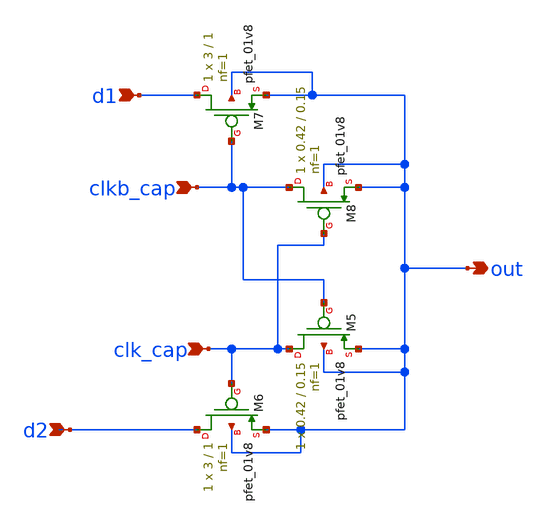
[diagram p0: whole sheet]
** sch_path: xschem/pmos_cp1.sch
**.subckt pmos_cp1 out clkb_cap d1 d2 clk_cap
*.opin out
*.ipin clkb_cap
*.ipin d1
*.ipin d2
*.ipin clk_cap
XM5 clk_cap clkb_cap out out sky130_fd_pr__pfet_01v8 L=0.15 W=0.42 nf=1 ad='int((nf+1)/2) * W/nf * 0.29'
+ as='int((nf+2)/2) * W/nf * 0.29' pd='2*int((nf+1)/2) * (W/nf + 0.29)' ps='2*int((nf+2)/2) * (W/nf + 0.29)'
+ nrd='0.29 / W' nrs='0.29 / W' sa=0 sb=0 sd=0 mult=1 m=1
XM6 d2 clk_cap out out sky130_fd_pr__pfet_01v8 L=1 W=3 nf=1 ad='int((nf+1)/2) * W/nf * 0.29' as='int((nf+2)/2) * W/nf * 0.29'
+ pd='2*int((nf+1)/2) * (W/nf + 0.29)' ps='2*int((nf+2)/2) * (W/nf + 0.29)' nrd='0.29 / W' nrs='0.29 / W'
+ sa=0 sb=0 sd=0 mult=1 m=1
XM7 d1 clkb_cap out out sky130_fd_pr__pfet_01v8 L=1 W=3 nf=1 ad='int((nf+1)/2) * W/nf * 0.29' as='int((nf+2)/2) * W/nf * 0.29'
+ pd='2*int((nf+1)/2) * (W/nf + 0.29)' ps='2*int((nf+2)/2) * (W/nf + 0.29)' nrd='0.29 / W' nrs='0.29 / W'
+ sa=0 sb=0 sd=0 mult=1 m=1
XM8 clkb_cap clk_cap out out sky130_fd_pr__pfet_01v8 L=0.15 W=0.42 nf=1 ad='int((nf+1)/2) * W/nf * 0.29'
+ as='int((nf+2)/2) * W/nf * 0.29' pd='2*int((nf+1)/2) * (W/nf + 0.29)' ps='2*int((nf+2)/2) * (W/nf + 0.29)'
+ nrd='0.29 / W' nrs='0.29 / W' sa=0 sb=0 sd=0 mult=1 m=1
**.ends
.end
